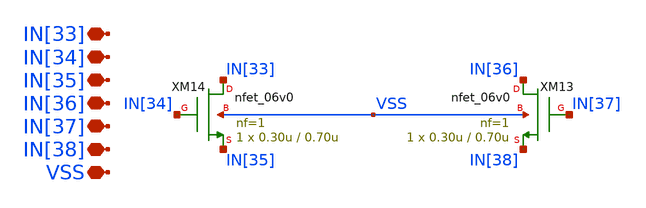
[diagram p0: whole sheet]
** sch_path: designs/libs/core_single-fet/nfet-vss/nfet-vss.sch
**.subckt nfet-vss VSS IN[33] IN[34] IN[35] IN[36] IN[37] IN[38]
*.iopin VSS
*.iopin IN[33]
*.iopin IN[34]
*.iopin IN[35]
*.iopin IN[36]
*.iopin IN[37]
*.iopin IN[38]
XM13 IN[36] IN[37] IN[38] VSS nfet_06v0 L=0.70u W=0.30u nf=1 ad='int((nf+1)/2) * W/nf * 0.18u' as='int((nf+2)/2) * W/nf * 0.18u'
+ pd='2*int((nf+1)/2) * (W/nf + 0.18u)' ps='2*int((nf+2)/2) * (W/nf + 0.18u)' nrd='0.18u / W' nrs='0.18u / W'
+ sa=0 sb=0 sd=0 m=1
XM14 IN[33] IN[34] IN[35] VSS nfet_06v0 L=0.70u W=0.30u nf=1 ad='int((nf+1)/2) * W/nf * 0.18u' as='int((nf+2)/2) * W/nf * 0.18u'
+ pd='2*int((nf+1)/2) * (W/nf + 0.18u)' ps='2*int((nf+2)/2) * (W/nf + 0.18u)' nrd='0.18u / W' nrs='0.18u / W'
+ sa=0 sb=0 sd=0 m=1
**.ends
.end
